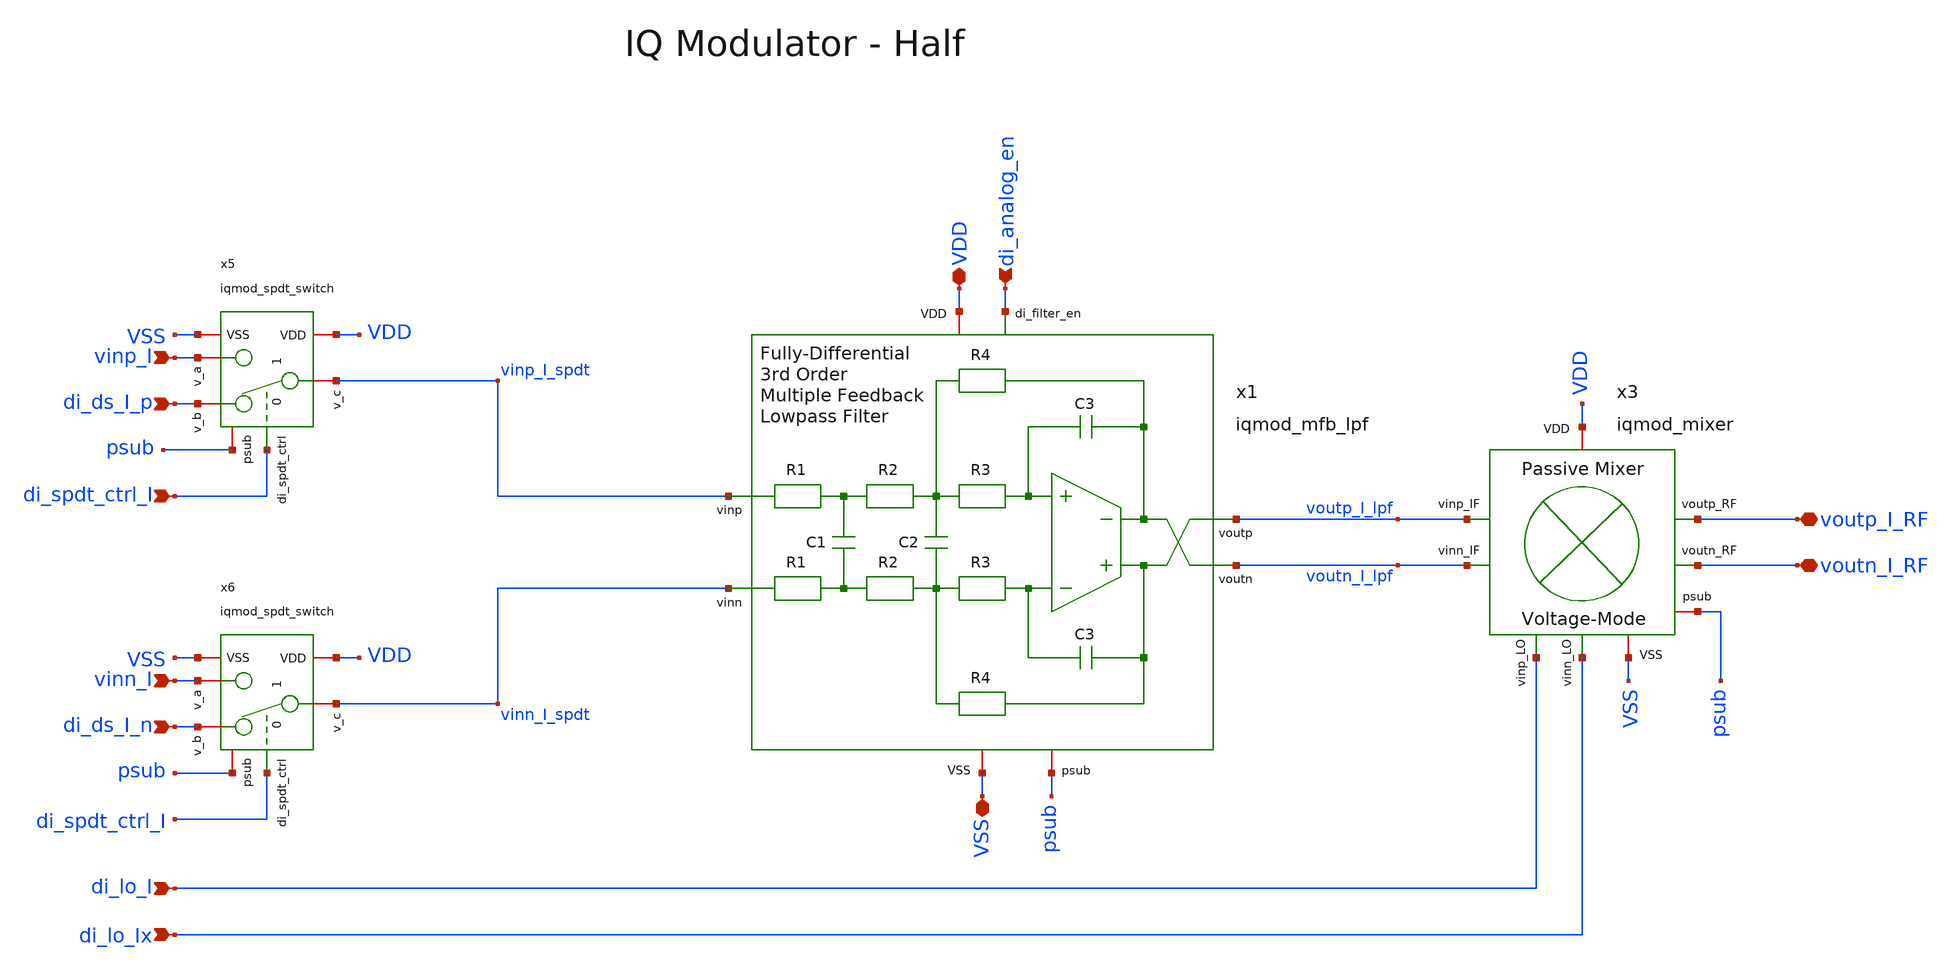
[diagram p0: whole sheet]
** sch_path: ihp130/macros/iqmod/xschem/iqmod_top_half.sch
**.subckt iqmod_top_half VDD voutp_I_RF VSS di_lo_I di_lo_Ix di_ds_I_p voutn_I_RF di_analog_en
*+ vinp_I vinn_I di_spdt_ctrl_I di_ds_I_n
*.iopin VDD
*.iopin voutp_I_RF
*.iopin VSS
*.ipin di_lo_I
*.ipin di_lo_Ix
*.ipin di_ds_I_p
*.iopin voutn_I_RF
*.ipin di_analog_en
*.ipin vinp_I
*.ipin vinn_I
*.ipin di_spdt_ctrl_I
*.ipin di_ds_I_n
x3 voutp_I_lpf voutn_I_lpf voutp_I_RF di_lo_I di_lo_Ix VDD VSS voutn_I_RF psub iqmod_mixer
x1 voutp_I_lpf vinp_I_spdt voutn_I_lpf vinn_I_spdt VDD VSS di_analog_en psub iqmod_mfb_lpf
x5 VDD di_spdt_ctrl_I VSS vinp_I_spdt di_ds_I_p vinp_I psub iqmod_spdt_switch
x6 VDD di_spdt_ctrl_I VSS vinn_I_spdt di_ds_I_n vinn_I psub iqmod_spdt_switch
**.ends
.end
